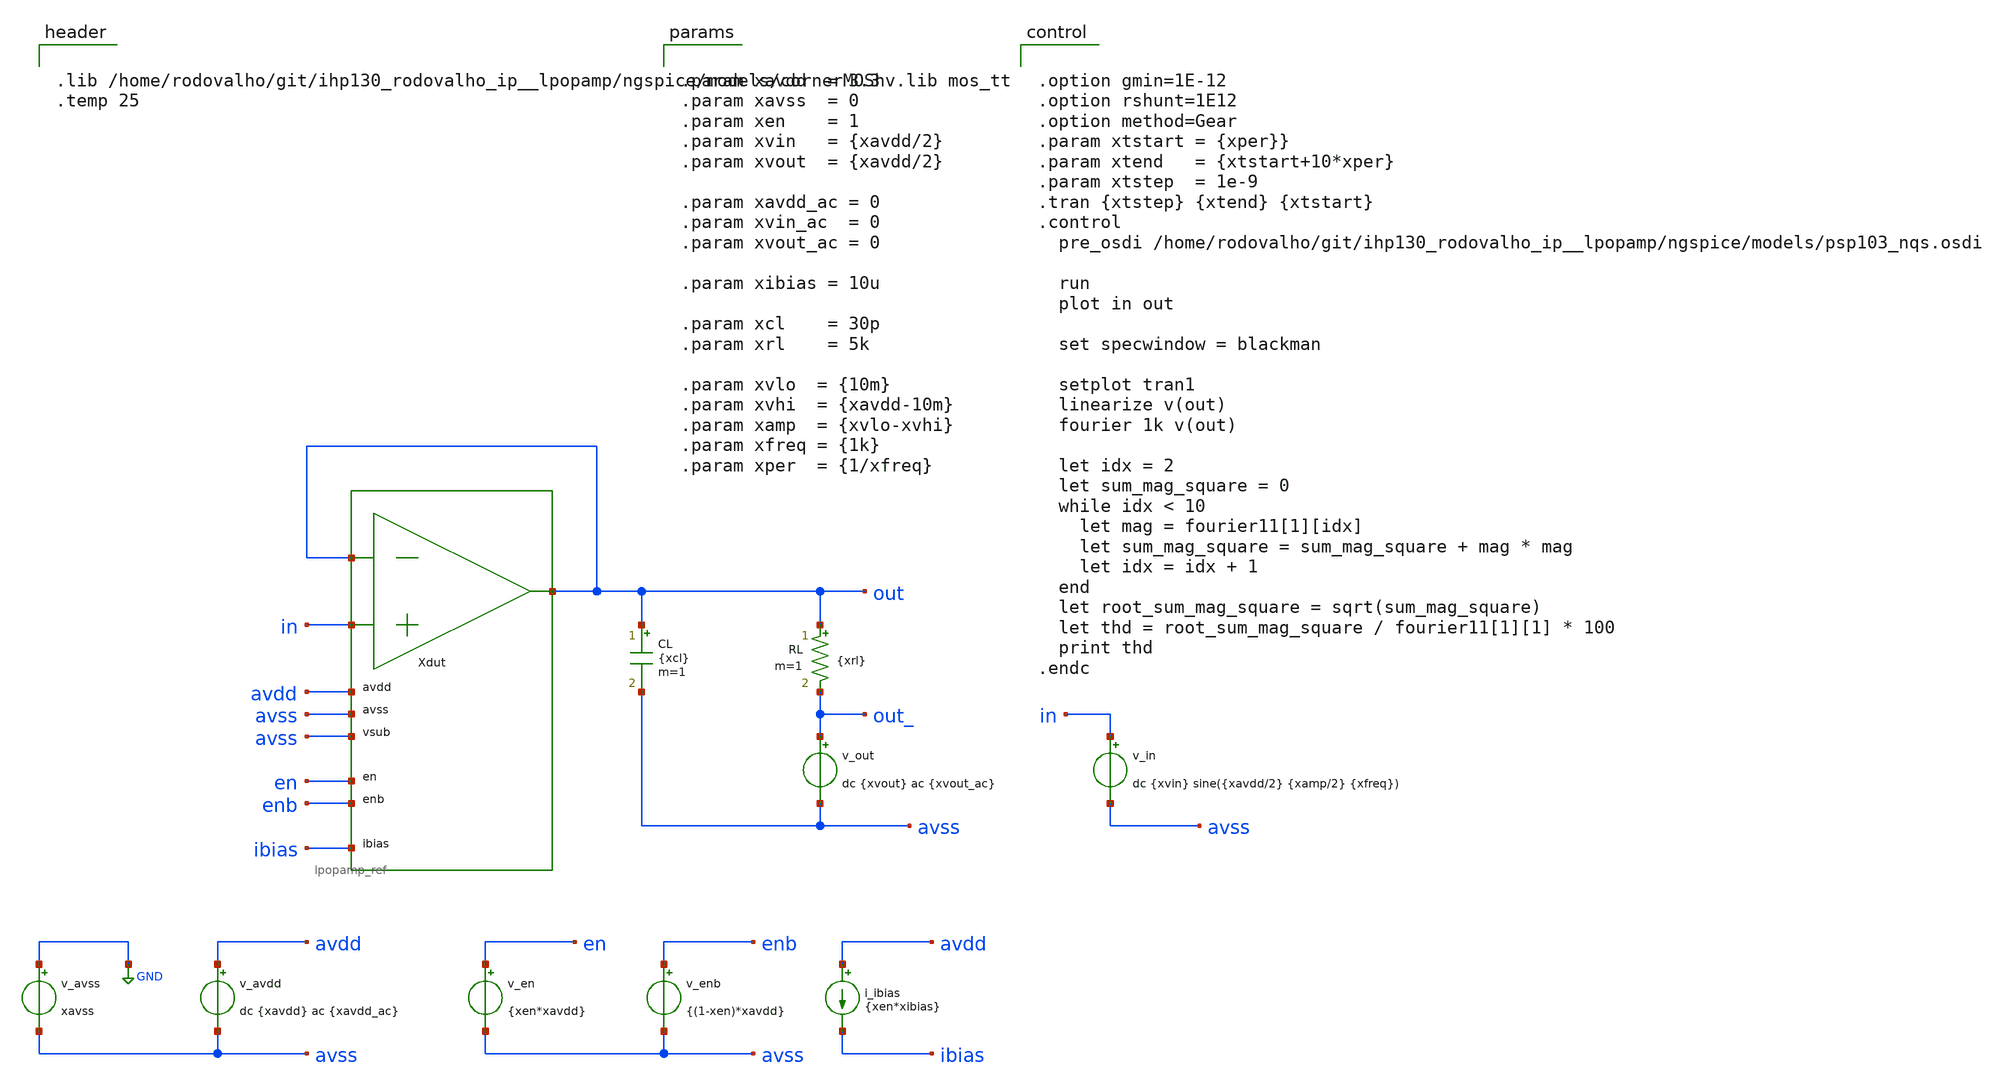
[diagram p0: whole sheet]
** sch_path: xschem/tb_lpopamp_buf_tran_sine.sch
**.subckt tb_lpopamp_buf_tran_sine
Xdut out in out avdd avss avss en enb ibias lpopamp_ref
v_avss GND avss xavss
v_avdd avdd avss dc {xavdd} ac {xavdd_ac}
v_in in avss dc {xvin} sine({xavdd/2} {xamp/2} {xfreq})
v_en en avss {xen*xavdd}
v_enb enb avss {(1-xen)*xavdd}
i_ibias avdd ibias {xen*xibias}
CL out avss {xcl} m=1
v_out out_ avss dc {xvout} ac {xvout_ac}
RL out out_ {xrl} m=1
**** begin user architecture code


.lib /home/rodovalho/git/ihp130_rodovalho_ip__lpopamp/ngspice/models/cornerMOShv.lib mos_tt
.temp 25




.option gmin=1E-12
.option rshunt=1E12
.option method=Gear
.param xtstart = {xper}}
.param xtend   = {xtstart+10*xper}
.param xtstep  = 1e-9
.tran {xtstep} {xtend} {xtstart}
.control
  pre_osdi /home/rodovalho/git/ihp130_rodovalho_ip__lpopamp/ngspice/models/psp103_nqs.osdi

  run
  plot in out

  set specwindow = blackman

  setplot tran1
  linearize v(out)
  fourier 1k v(out)

  let idx = 2
  let sum_mag_square = 0
  while idx < 10
    let mag = fourier11[1][idx]
    let sum_mag_square = sum_mag_square + mag * mag
    let idx = idx + 1
  end
  let root_sum_mag_square = sqrt(sum_mag_square)
  let thd = root_sum_mag_square / fourier11[1][1] * 100
  print thd
.endc




.param xavdd  = 3.3
.param xavss  = 0
.param xen    = 1
.param xvin   = {xavdd/2}
.param xvout  = {xavdd/2}

.param xavdd_ac = 0
.param xvin_ac  = 0
.param xvout_ac = 0

.param xibias = 10u

.param xcl    = 30p
.param xrl    = 5k

.param xvlo  = {10m}
.param xvhi  = {xavdd-10m}
.param xamp  = {xvlo-xvhi}
.param xfreq = {1k}
.param xper  = {1/xfreq}


**** end user architecture code
**.ends
.GLOBAL GND
.end
